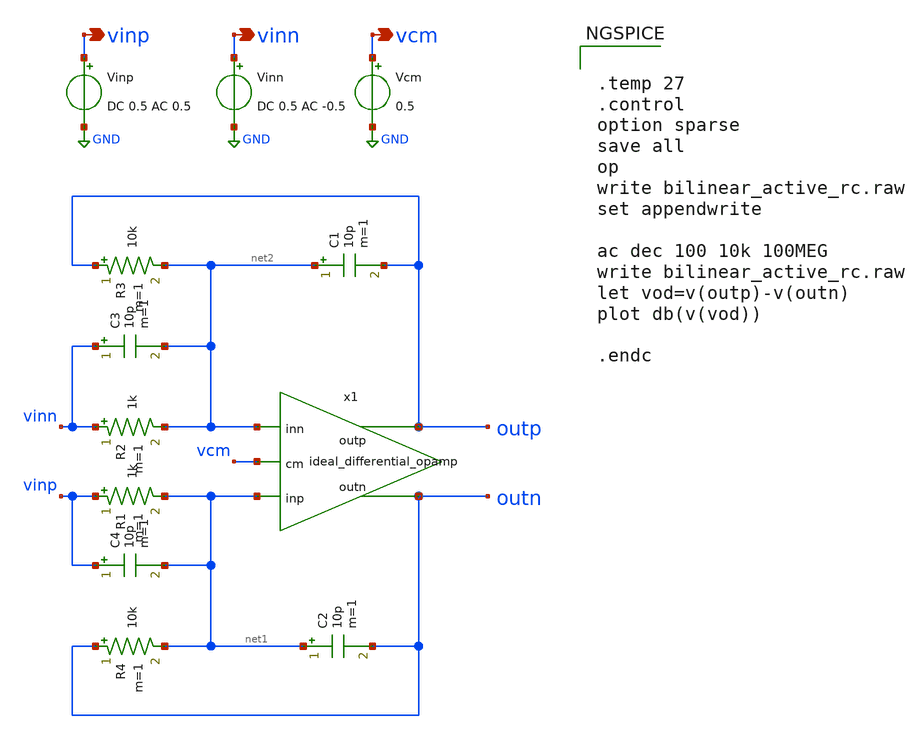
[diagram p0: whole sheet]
** sch_path: prj/template/2_Idealized_circuits/bilinear_active_rc.sch
**.subckt bilinear_active_rc vinp vinn vcm
*.opin vinp
*.opin vinn
*.opin vcm
C1 net2 outp 10p m=1
Vinp vinp GND DC 0.5 AC 0.5
Vinn vinn GND DC 0.5 AC -0.5
Vcm vcm GND 0.5
x1 net1 net2 outp outn vcm ideal_differential_opamp
R1 vinp net1 1k m=1
R2 vinn net2 1k m=1
R3 outp net2 10k m=1
R4 outn net1 10k m=1
C2 net1 outn 10p m=1
C3 vinn net2 10p m=1
C4 vinp net1 10p m=1
**** begin user architecture code


.temp 27
.control
option sparse
save all
op
write bilinear_active_rc.raw
set appendwrite

ac dec 100 10k 100MEG
write bilinear_active_rc.raw
let vod=v(outp)-v(outn)
plot db(v(vod))

.endc


**** end user architecture code
**.ends

* expanding   symbol:  ideal_differential_opamp.sym # of pins=5
** sym_path: prj/template/2_Idealized_circuits/ideal_differential_opamp.sym
** sch_path: prj/template/2_Idealized_circuits/ideal_differential_opamp.sch
.subckt ideal_differential_opamp inp inn outp outn cm
*.opin outp
*.ipin inp
*.ipin inn
*.opin outn
*.ipin cm
G1 outp net1 inp inn 100Meg
R1 outp net1 1 m=1
G2 net1 outn inp inn 100Meg
R2 net1 outn 1 m=1
G3 net1 GND cm net1 100Meg
.ends

.GLOBAL GND
.end
